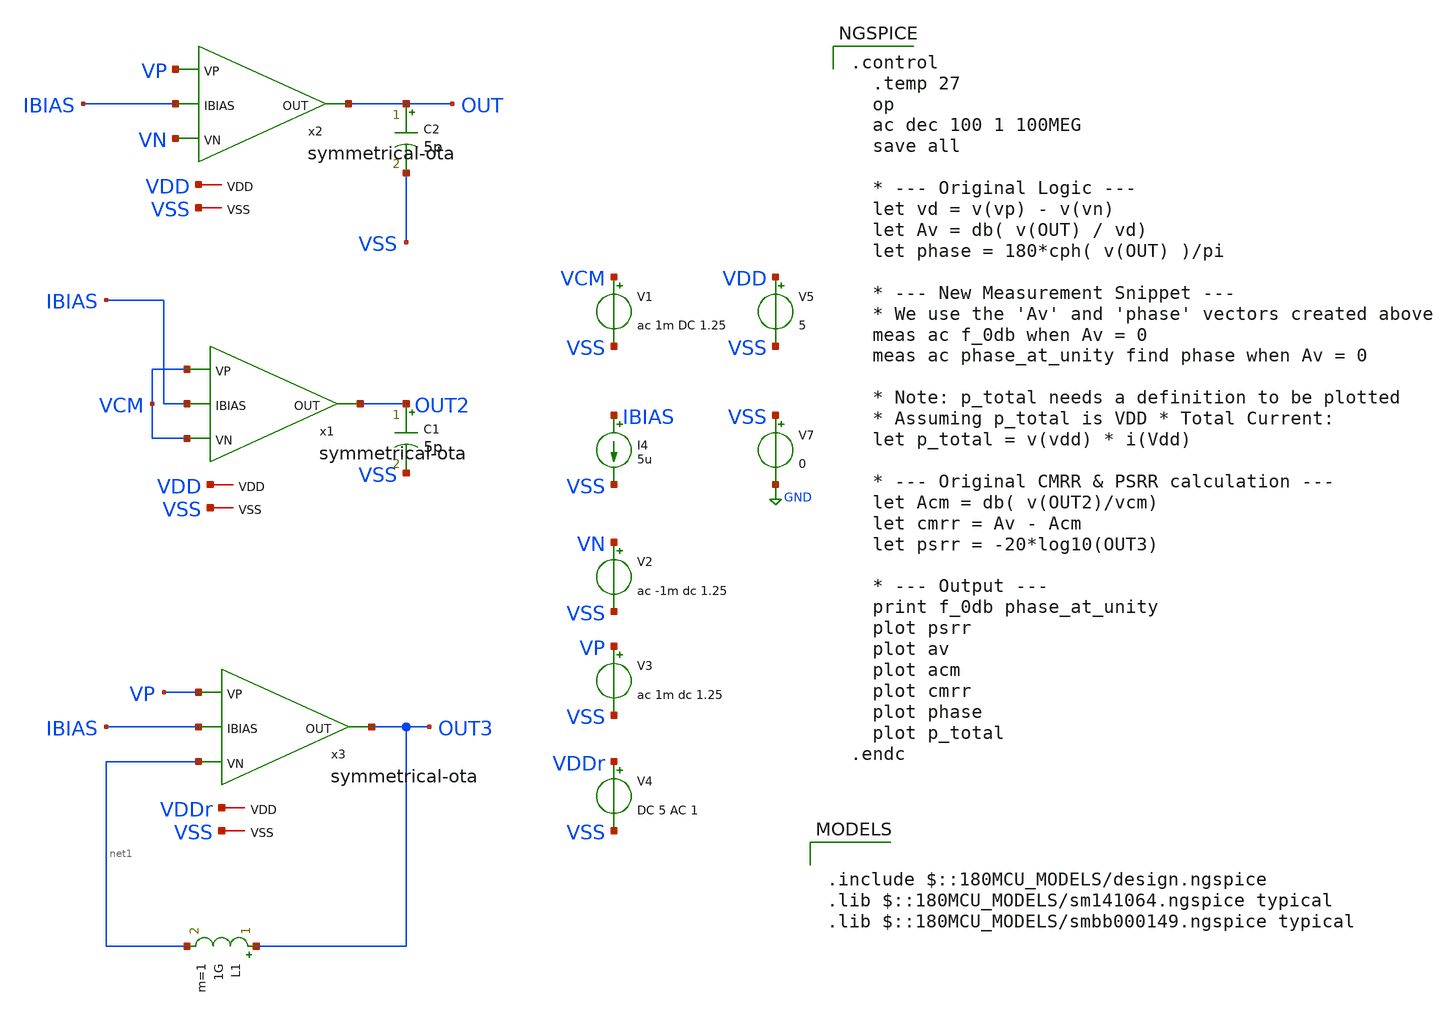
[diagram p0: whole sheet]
** sch_path: designs/symmetrical-ota/tb-ac.sch.sch
**.subckt tb-ac.sch
V2 VN VSS ac -1m dc 1.25
V3 VP VSS ac 1m dc 1.25
V5 VDD VSS 5
V7 VSS GND 0
C2 OUT VSS 5p m=1
I4 IBIAS VSS 5u
C1 OUT2 VSS 5p m=1
V1 VCM VSS ac 1m DC 1.25
V4 VDDr VSS DC 5 AC 1
L1 OUT3 net1 1G m=1
x1 VDD VCM VCM IBIAS OUT2 VSS symmetrical-ota
x2 VDD VP VN IBIAS OUT VSS symmetrical-ota
x3 VDDr VP net1 IBIAS OUT3 VSS symmetrical-ota
**** begin user architecture code

.control
  .temp 27
  op
  ac dec 100 1 100MEG
  save all

  * --- Original Logic ---
  let vd = v(vp) - v(vn)
  let Av = db( v(OUT) / vd)
  let phase = 180*cph( v(OUT) )/pi

  * --- New Measurement Snippet ---
  * We use the 'Av' and 'phase' vectors created above
  meas ac f_0db when Av = 0
  meas ac phase_at_unity find phase when Av = 0

  * Note: p_total needs a definition to be plotted
  * Assuming p_total is VDD * Total Current:
  let p_total = v(vdd) * i(Vdd)

  * --- Original CMRR & PSRR calculation ---
  let Acm = db( v(OUT2)/vcm)
  let cmrr = Av - Acm
  let psrr = -20*log10(OUT3)

  * --- Output ---
  print f_0db phase_at_unity
  plot psrr
  plot av
  plot acm
  plot cmrr
  plot phase
  plot p_total
.endc




.include $::180MCU_MODELS/design.ngspice
.lib $::180MCU_MODELS/sm141064.ngspice typical
.lib $::180MCU_MODELS/smbb000149.ngspice typical

**** end user architecture code
**.ends

* expanding   symbol:
*+  /foss/designs/2026/buck-gf180-test/designs/symmetrical-ota/symmetrical-ota.sym # of pins=6
** sym_path: designs/symmetrical-ota/symmetrical-ota.sym
** sch_path: designs/symmetrical-ota/symmetrical-ota.sch
.subckt symmetrical-ota VDD VP VN IBIAS OUT VSS
*.ipin IBIAS
*.ipin VN
*.ipin VP
*.opin OUT
*.iopin VDD
*.iopin VSS
XM1 net3 VN net1 VDD pfet_05v0 L=0.9u W=10.5u nf=4 ad='int((nf+1)/2) * W/nf * 0.18u' as='int((nf+2)/2) * W/nf * 0.18u'
+ pd='2*int((nf+1)/2) * (W/nf + 0.18u)' ps='2*int((nf+2)/2) * (W/nf + 0.18u)' nrd='0.18u / W' nrs='0.18u / W'
+ sa=0 sb=0 sd=0 m=1
XM2 net2 VP net1 VDD pfet_05v0 L=0.9u W=10.5u nf=4 ad='int((nf+1)/2) * W/nf * 0.18u' as='int((nf+2)/2) * W/nf * 0.18u'
+ pd='2*int((nf+1)/2) * (W/nf + 0.18u)' ps='2*int((nf+2)/2) * (W/nf + 0.18u)' nrd='0.18u / W' nrs='0.18u / W'
+ sa=0 sb=0 sd=0 m=1
XM3 net1 IBIAS VDD VDD pfet_05v0 L=1u W=15u nf=4 ad='int((nf+1)/2) * W/nf * 0.18u' as='int((nf+2)/2) * W/nf * 0.18u'
+ pd='2*int((nf+1)/2) * (W/nf + 0.18u)' ps='2*int((nf+2)/2) * (W/nf + 0.18u)' nrd='0.18u / W' nrs='0.18u / W'
+ sa=0 sb=0 sd=0 m=1
XM4 IBIAS IBIAS VDD VDD pfet_05v0 L=1u W=15u nf=4 ad='int((nf+1)/2) * W/nf * 0.18u' as='int((nf+2)/2) * W/nf * 0.18u'
+ pd='2*int((nf+1)/2) * (W/nf + 0.18u)' ps='2*int((nf+2)/2) * (W/nf + 0.18u)' nrd='0.18u / W' nrs='0.18u / W'
+ sa=0 sb=0 sd=0 m=1
XM5 net2 net2 VSS VSS nfet_05v0 L=0.75u W=2.17u nf=1 ad='int((nf+1)/2) * W/nf * 0.18u' as='int((nf+2)/2) * W/nf * 0.18u'
+ pd='2*int((nf+1)/2) * (W/nf + 0.18u)' ps='2*int((nf+2)/2) * (W/nf + 0.18u)' nrd='0.18u / W' nrs='0.18u / W'
+ sa=0 sb=0 sd=0 m=1
XM6 net3 net3 VSS VSS nfet_05v0 L=0.75u W=2.17u nf=1 ad='int((nf+1)/2) * W/nf * 0.18u' as='int((nf+2)/2) * W/nf * 0.18u'
+ pd='2*int((nf+1)/2) * (W/nf + 0.18u)' ps='2*int((nf+2)/2) * (W/nf + 0.18u)' nrd='0.18u / W' nrs='0.18u / W'
+ sa=0 sb=0 sd=0 m=1
XM7 OUT net4 VDD VDD pfet_05v0 L=1u W=9.4u nf=4 ad='int((nf+1)/2) * W/nf * 0.18u' as='int((nf+2)/2) * W/nf * 0.18u'
+ pd='2*int((nf+1)/2) * (W/nf + 0.18u)' ps='2*int((nf+2)/2) * (W/nf + 0.18u)' nrd='0.18u / W' nrs='0.18u / W'
+ sa=0 sb=0 sd=0 m=1
XM8 net4 net4 VDD VDD pfet_05v0 L=1u W=9.4u nf=4 ad='int((nf+1)/2) * W/nf * 0.18u' as='int((nf+2)/2) * W/nf * 0.18u'
+ pd='2*int((nf+1)/2) * (W/nf + 0.18u)' ps='2*int((nf+2)/2) * (W/nf + 0.18u)' nrd='0.18u / W' nrs='0.18u / W'
+ sa=0 sb=0 sd=0 m=1
XM9 net4 net3 VSS VSS nfet_05v0 L=0.75u W=2.17u nf=1 ad='int((nf+1)/2) * W/nf * 0.18u' as='int((nf+2)/2) * W/nf * 0.18u'
+ pd='2*int((nf+1)/2) * (W/nf + 0.18u)' ps='2*int((nf+2)/2) * (W/nf + 0.18u)' nrd='0.18u / W' nrs='0.18u / W'
+ sa=0 sb=0 sd=0 m=1
XM10 OUT net2 VSS VSS nfet_05v0 L=0.75u W=2.17u nf=1 ad='int((nf+1)/2) * W/nf * 0.18u' as='int((nf+2)/2) * W/nf * 0.18u'
+ pd='2*int((nf+1)/2) * (W/nf + 0.18u)' ps='2*int((nf+2)/2) * (W/nf + 0.18u)' nrd='0.18u / W' nrs='0.18u / W'
+ sa=0 sb=0 sd=0 m=1
.ends

.GLOBAL GND
.end
